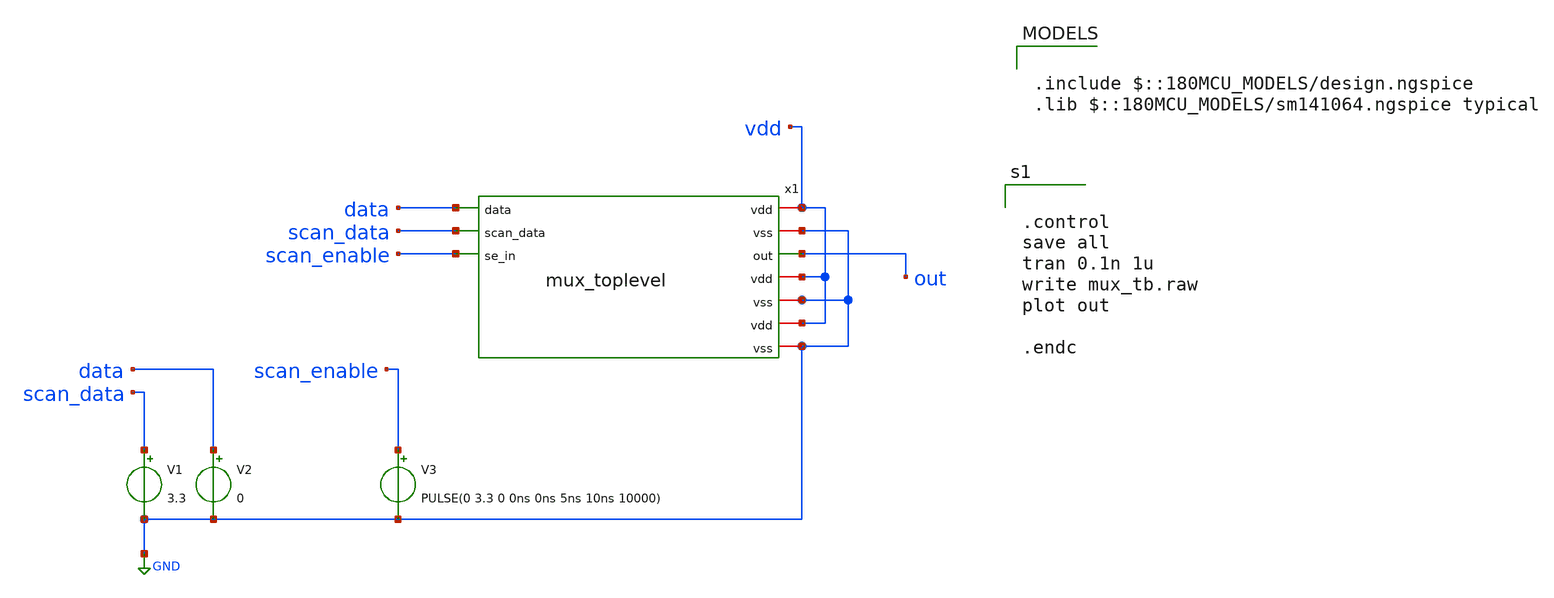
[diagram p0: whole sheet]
** sch_path: designs/schematics/mux2x1_transmission_gate/mux_tb.sch
**.subckt mux_tb
V1 scan_data GND 3.3
V2 data GND 0
V3 scan_enable GND PULSE(0 3.3 0 0ns 0ns 5ns 10ns 10000)
x1 vdd data GND out scan_data scan_enable mux_toplevel
**** begin user architecture code

.include $::180MCU_MODELS/design.ngspice
.lib $::180MCU_MODELS/sm141064.ngspice typical



.control
save all
tran 0.1n 1u
write mux_tb.raw
plot out

.endc


**** end user architecture code
**.ends

* expanding   symbol:  schematics/mux2x1_transmission_gate/mux_toplevel.sym # of pins=10
** sym_path: designs/schematics/mux2x1_transmission_gate/mux_toplevel.sym
** sch_path: designs/schematics/mux2x1_transmission_gate/mux_toplevel.sch
.subckt mux_toplevel vdd data vss out scan_data se_in
*.iopin vdd
*.opin out
*.ipin data
*.ipin scan_data
*.ipin se_in
*.iopin vdd
*.iopin vss
*.iopin vss
*.iopin vdd
*.iopin vss
x2 vdd data net1 out se_in vss mux_tg
x3 vdd scan_data se_in out net1 vss mux_tg
x1 vdd se_in net1 vss mux_ctrl_logic
.ends


* expanding   symbol:  schematics/mux2x1_transmission_gate/mux_tg.sym # of pins=6
** sym_path: designs/cells/sdffrq/sch/mux_tg.sym
** sch_path: designs/cells/sdffrq/sch/mux_tg.sch
.subckt mux_tg VDD P_GATE IN OUT N_GATE VSS
*.iopin VDD
*.iopin VSS
*.opin OUT
*.ipin IN
*.ipin P_GATE
*.ipin N_GATE
XM1 IN N_GATE OUT VSS nfet_03v3 L=0.3u W=0.85u nf=1 ad='int((nf+1)/2) * W/nf * 0.18u' as='int((nf+2)/2) * W/nf * 0.18u'
+ pd='2*int((nf+1)/2) * (W/nf + 0.18u)' ps='2*int((nf+2)/2) * (W/nf + 0.18u)' nrd='0.18u / W' nrs='0.18u / W'
+ sa=0 sb=0 sd=0 m=1
XM2 IN P_GATE OUT VDD pfet_03v3 L=0.3u W=1.7u nf=1 ad='int((nf+1)/2) * W/nf * 0.18u' as='int((nf+2)/2) * W/nf * 0.18u'
+ pd='2*int((nf+1)/2) * (W/nf + 0.18u)' ps='2*int((nf+2)/2) * (W/nf + 0.18u)' nrd='0.18u / W' nrs='0.18u / W'
+ sa=0 sb=0 sd=0 m=1
.ends


* expanding   symbol:  schematics/mux2x1_transmission_gate/mux_ctrl_logic.sym # of pins=4
** sym_path: designs/schematics/mux2x1_transmission_gate/mux_ctrl_logic.sym
** sch_path: designs/schematics/mux2x1_transmission_gate/mux_ctrl_logic.sch
.subckt mux_ctrl_logic vdd in out_inv gnd
*.iopin vdd
*.iopin gnd
*.iopin out_inv
*.iopin in
XM1 out_inv in gnd gnd nfet_03v3 L=0.28u W=0.22u nf=1 ad='int((nf+1)/2) * W/nf * 0.18u' as='int((nf+2)/2) * W/nf * 0.18u'
+ pd='2*int((nf+1)/2) * (W/nf + 0.18u)' ps='2*int((nf+2)/2) * (W/nf + 0.18u)' nrd='0.18u / W' nrs='0.18u / W'
+ sa=0 sb=0 sd=0 m=1
XM2 out_inv in vdd vdd pfet_03v3 L=0.28u W=0.22u nf=1 ad='int((nf+1)/2) * W/nf * 0.18u' as='int((nf+2)/2) * W/nf * 0.18u'
+ pd='2*int((nf+1)/2) * (W/nf + 0.18u)' ps='2*int((nf+2)/2) * (W/nf + 0.18u)' nrd='0.18u / W' nrs='0.18u / W'
+ sa=0 sb=0 sd=0 m=1
.ends

.GLOBAL GND
.end
